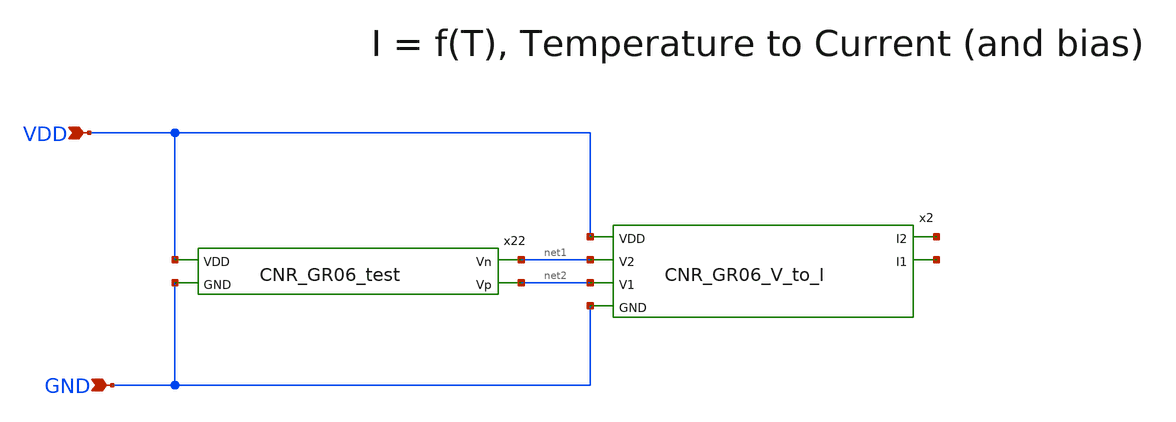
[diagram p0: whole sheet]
** sch_path: design/CNR_GR06_SKY130NM/CNR_GR06.sch
**.subckt CNR_GR06 VDD GND
*.ipin VDD
*.ipin GND
x22 VDD net1 net2 GND CNR_GR06_test
x2 VDD net3 net4 net1 net2 GND CNR_GR06_V_to_I
**.ends
.end
